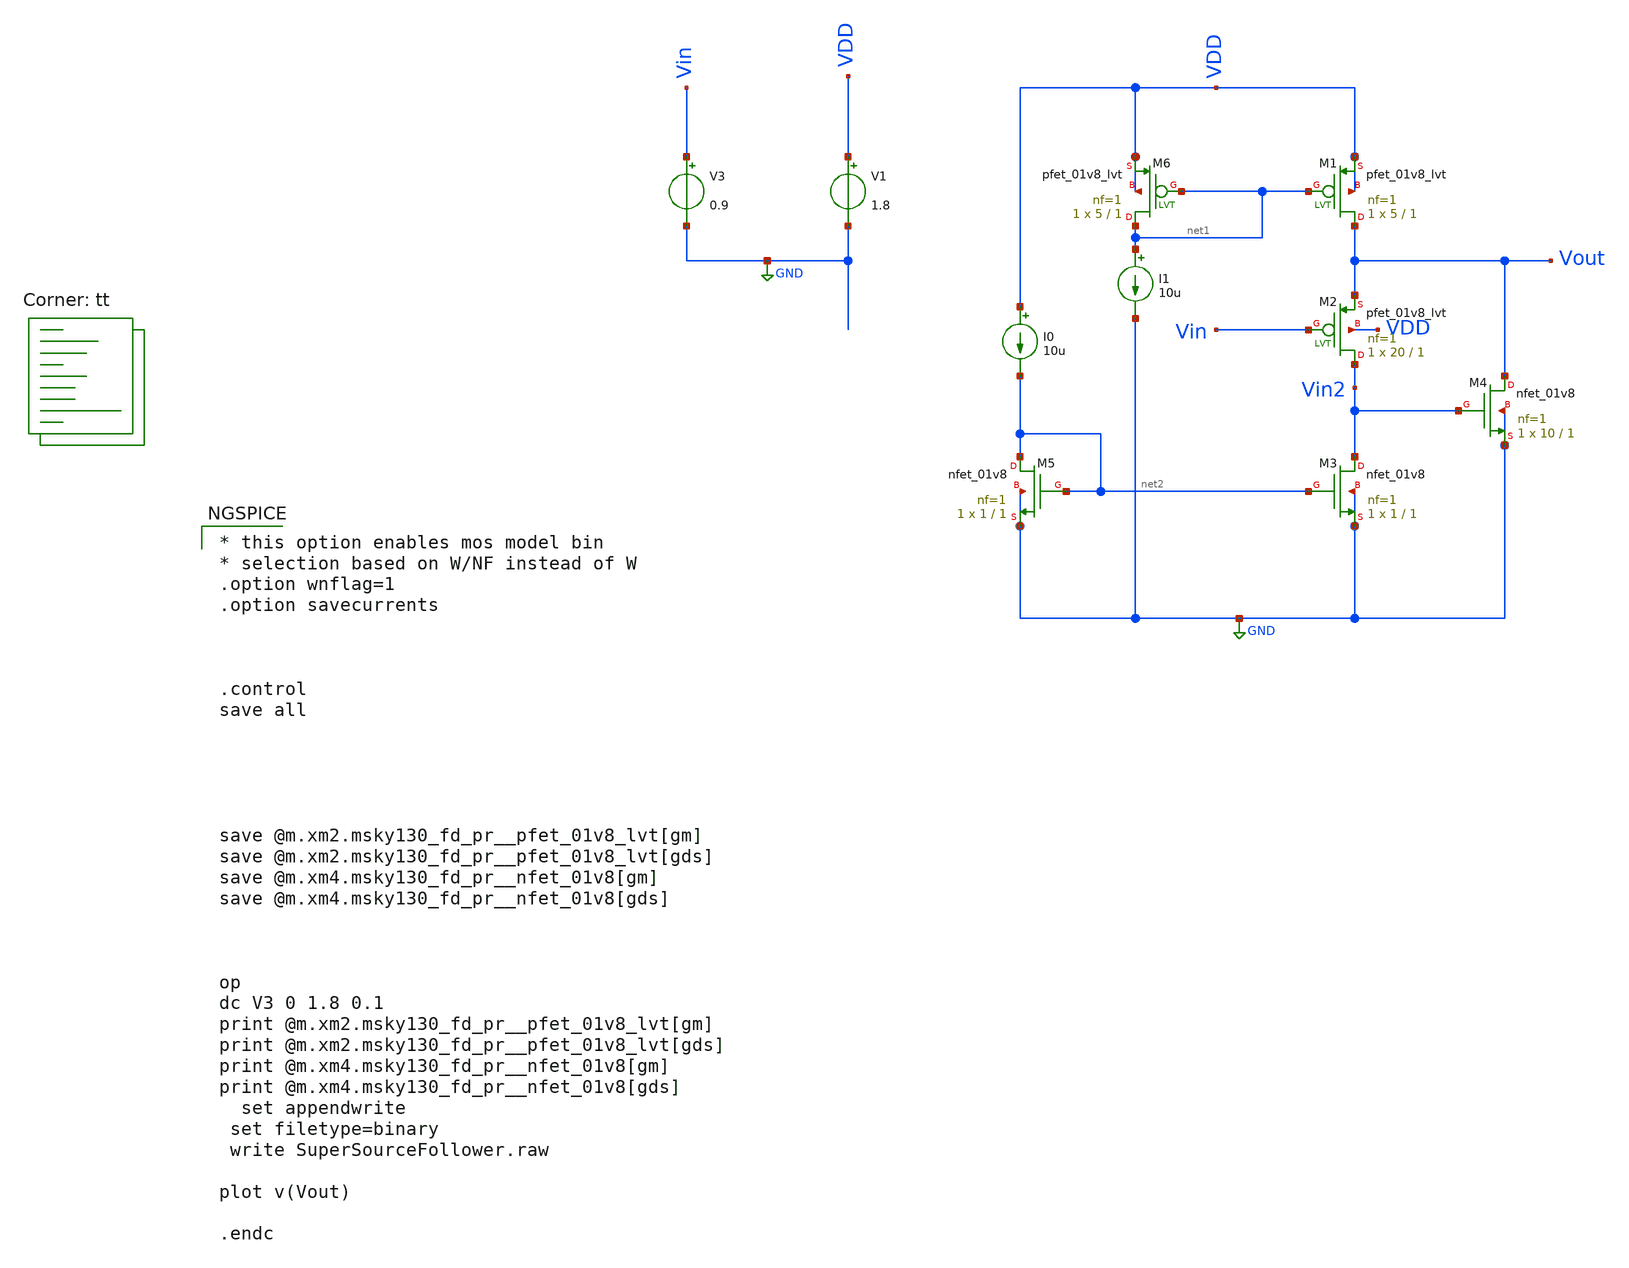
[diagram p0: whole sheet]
** sch_path: userLib/SuperSourceFollower.sch
**.subckt SuperSourceFollower
XM1 Vout net1 VDD VDD sky130_fd_pr__pfet_01v8_lvt L=1 W=5 nf=1 ad='int((nf+1)/2) * W/nf * 0.29' as='int((nf+2)/2) * W/nf * 0.29'
+ pd='2*int((nf+1)/2) * (W/nf + 0.29)' ps='2*int((nf+2)/2) * (W/nf + 0.29)' nrd='0.29 / W' nrs='0.29 / W'
+ sa=0 sb=0 sd=0 mult=1 m=1
XM2 Vin2 Vin Vout VDD sky130_fd_pr__pfet_01v8_lvt L=1 W=20 nf=1 ad='int((nf+1)/2) * W/nf * 0.29' as='int((nf+2)/2) * W/nf * 0.29'
+ pd='2*int((nf+1)/2) * (W/nf + 0.29)' ps='2*int((nf+2)/2) * (W/nf + 0.29)' nrd='0.29 / W' nrs='0.29 / W'
+ sa=0 sb=0 sd=0 mult=1 m=1
XM3 Vin2 net2 GND GND sky130_fd_pr__nfet_01v8 L=1 W=1 nf=1 ad='int((nf+1)/2) * W/nf * 0.29' as='int((nf+2)/2) * W/nf * 0.29'
+ pd='2*int((nf+1)/2) * (W/nf + 0.29)' ps='2*int((nf+2)/2) * (W/nf + 0.29)' nrd='0.29 / W' nrs='0.29 / W'
+ sa=0 sb=0 sd=0 mult=1 m=1
XM4 Vout Vin2 GND GND sky130_fd_pr__nfet_01v8 L=1 W=10 nf=1 ad='int((nf+1)/2) * W/nf * 0.29' as='int((nf+2)/2) * W/nf * 0.29'
+ pd='2*int((nf+1)/2) * (W/nf + 0.29)' ps='2*int((nf+2)/2) * (W/nf + 0.29)' nrd='0.29 / W' nrs='0.29 / W'
+ sa=0 sb=0 sd=0 mult=1 m=1
XM5 net2 net2 GND GND sky130_fd_pr__nfet_01v8 L=1 W=1 nf=1 ad='int((nf+1)/2) * W/nf * 0.29' as='int((nf+2)/2) * W/nf * 0.29'
+ pd='2*int((nf+1)/2) * (W/nf + 0.29)' ps='2*int((nf+2)/2) * (W/nf + 0.29)' nrd='0.29 / W' nrs='0.29 / W'
+ sa=0 sb=0 sd=0 mult=1 m=1
XM6 net1 net1 VDD VDD sky130_fd_pr__pfet_01v8_lvt L=1 W=5 nf=1 ad='int((nf+1)/2) * W/nf * 0.29' as='int((nf+2)/2) * W/nf * 0.29'
+ pd='2*int((nf+1)/2) * (W/nf + 0.29)' ps='2*int((nf+2)/2) * (W/nf + 0.29)' nrd='0.29 / W' nrs='0.29 / W'
+ sa=0 sb=0 sd=0 mult=1 m=1
I0 VDD net2 10u
I1 net1 GND 10u
V1 VDD GND 1.8
V3 Vin GND 0.9
**** begin user architecture code
.lib $::SKYWATER_MODELS/sky130.lib.spice tt

* this option enables mos model bin
* selection based on W/NF instead of W
.option wnflag=1
.option savecurrents



.control
save all





save @m.xm2.msky130_fd_pr__pfet_01v8_lvt[gm]
save @m.xm2.msky130_fd_pr__pfet_01v8_lvt[gds]
save @m.xm4.msky130_fd_pr__nfet_01v8[gm]
save @m.xm4.msky130_fd_pr__nfet_01v8[gds]



op
dc V3 0 1.8 0.1
print @m.xm2.msky130_fd_pr__pfet_01v8_lvt[gm]
print @m.xm2.msky130_fd_pr__pfet_01v8_lvt[gds]
print @m.xm4.msky130_fd_pr__nfet_01v8[gm]
print @m.xm4.msky130_fd_pr__nfet_01v8[gds]
  set appendwrite
 set filetype=binary
 write SuperSourceFollower.raw

plot v(Vout)

.endc



**** end user architecture code
**.ends
.GLOBAL GND
.end
